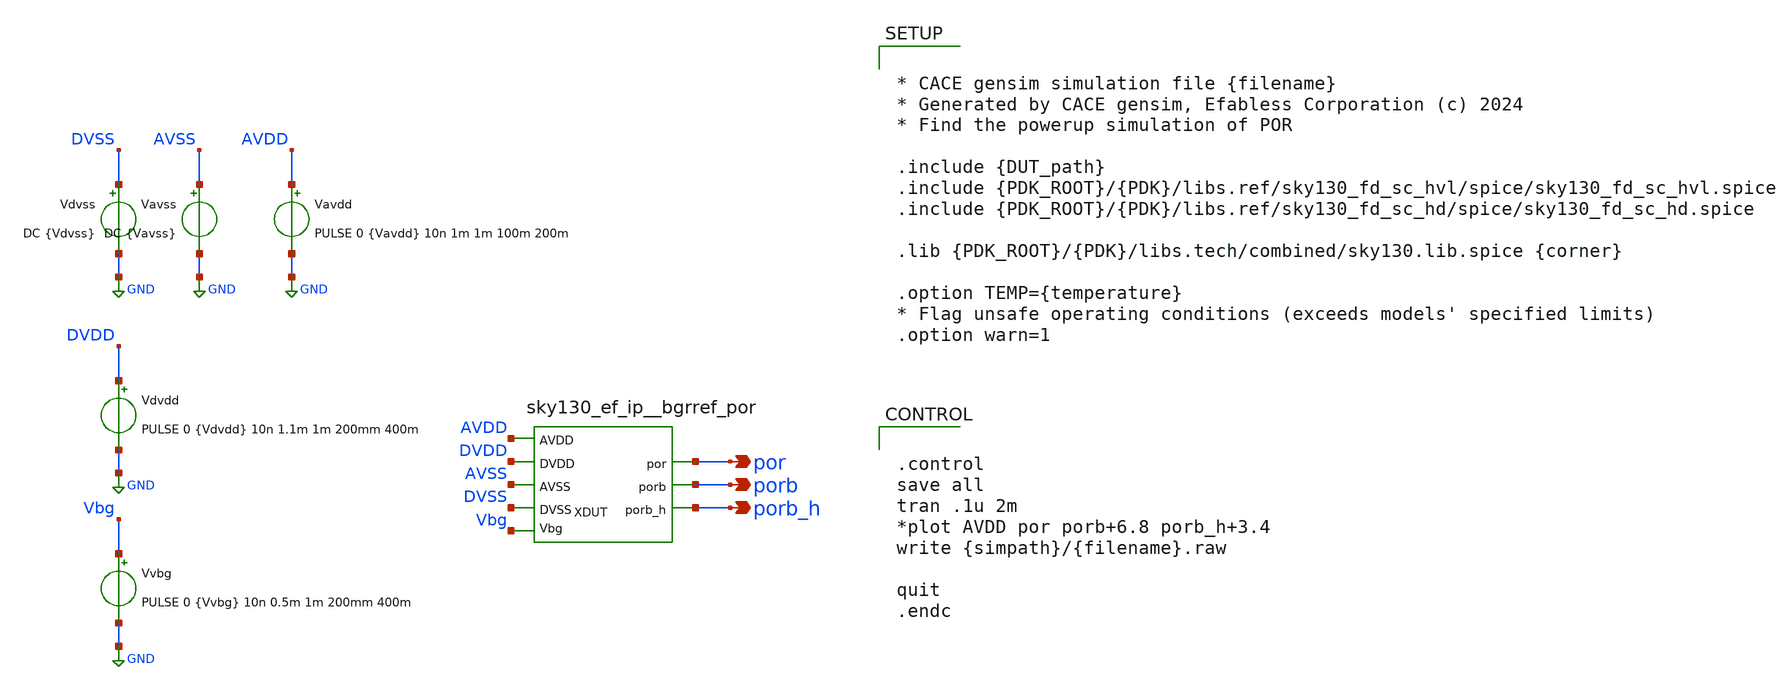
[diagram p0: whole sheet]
** sch_path: xschem/sky130_ef_ip__bgrref_por_tb1.sch
**.subckt sky130_ef_ip__bgrref_por_tb1 por porb porb_h
*.opin por
*.opin porb
*.opin porb_h
XDUT Vbg por AVSS AVDD DVDD porb DVSS porb_h VCC VSS sky130_ef_ip__bgrref_por W_N=1 L_N=0.2 W_P=1
+ L_P=0.2 m=1
Vdvss DVSS GND DC {Vdvss}
Vavdd AVDD GND PULSE 0 {Vavdd} 10n 1m 1m 100m 200m
Vavss AVSS GND DC {Vavss}
Vdvdd DVDD GND PULSE 0 {Vdvdd} 10n 1.1m 1m 200mm 400m
Vvbg Vbg GND PULSE 0 {Vvbg} 10n 0.5m 1m 200mm 400m
**** begin user architecture code


* CACE gensim simulation file {filename}
* Generated by CACE gensim, Efabless Corporation (c) 2024
* Find the powerup simulation of POR

.include {DUT_path}
.include {PDK_ROOT}/{PDK}/libs.ref/sky130_fd_sc_hvl/spice/sky130_fd_sc_hvl.spice
.include {PDK_ROOT}/{PDK}/libs.ref/sky130_fd_sc_hd/spice/sky130_fd_sc_hd.spice

.lib {PDK_ROOT}/{PDK}/libs.tech/combined/sky130.lib.spice {corner}

.option TEMP={temperature}
* Flag unsafe operating conditions (exceeds models' specified limits)
.option warn=1




.control
save all
tran .1u 2m
*plot AVDD por porb+6.8 porb_h+3.4
write {simpath}/{filename}.raw

quit
.endc


**** end user architecture code
**.ends
.GLOBAL GND
.end
